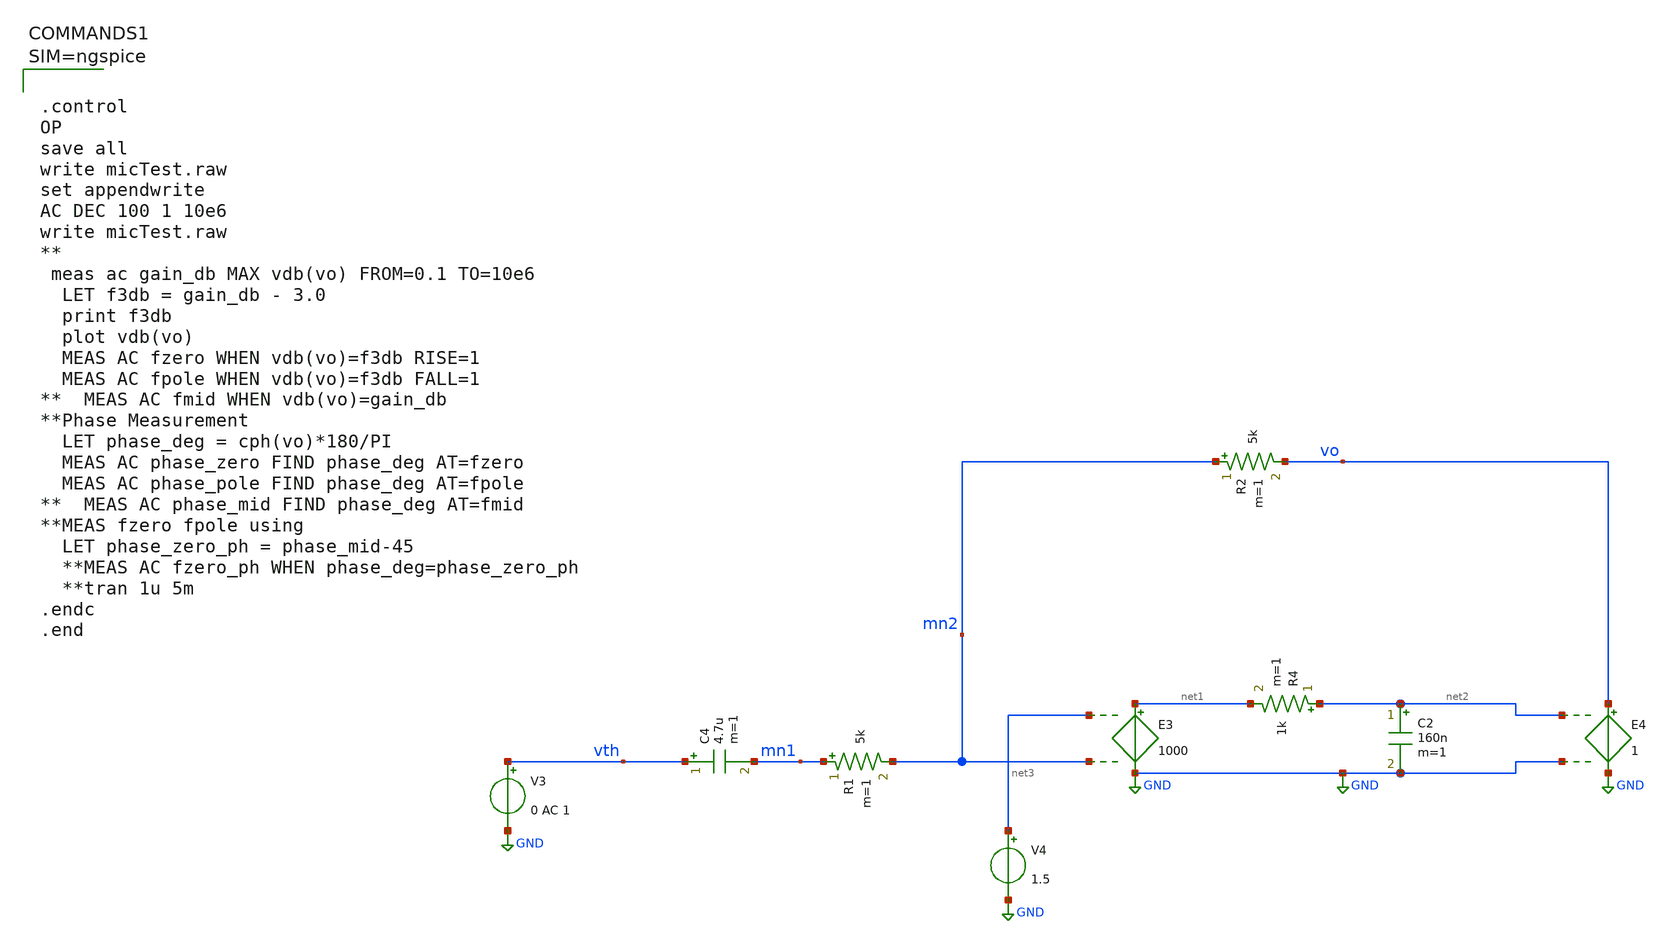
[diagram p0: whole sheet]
** sch_path: xschem/micNewopa_mod3.sch
**.subckt micNewopa_mod3
V3 vth GND 0 AC 1
V4 net3 GND 1.5
R1 mn1 mn2 5k m=1
R2 mn2 vo 5k m=1
C4 vth mn1 4.7u m=1
E3 net1 GND net3 mn2 1000
E4 vo GND net2 GND 1
R4 net2 net1 1k m=1
C2 net2 GND 160n m=1
**** begin user architecture code



.control
OP
save all
write micTest.raw
set appendwrite
AC DEC 100 1 10e6
write micTest.raw
**
 meas ac gain_db MAX vdb(vo) FROM=0.1 TO=10e6
  LET f3db = gain_db - 3.0
  print f3db
  plot vdb(vo)
  MEAS AC fzero WHEN vdb(vo)=f3db RISE=1
  MEAS AC fpole WHEN vdb(vo)=f3db FALL=1
**  MEAS AC fmid WHEN vdb(vo)=gain_db
**Phase Measurement
  LET phase_deg = cph(vo)*180/PI
  MEAS AC phase_zero FIND phase_deg AT=fzero
  MEAS AC phase_pole FIND phase_deg AT=fpole
**  MEAS AC phase_mid FIND phase_deg AT=fmid
**MEAS fzero fpole using
  LET phase_zero_ph = phase_mid-45
  **MEAS AC fzero_ph WHEN phase_deg=phase_zero_ph
  **tran 1u 5m
.endc
.end



**** end user architecture code
**.ends
.GLOBAL GND
.end
